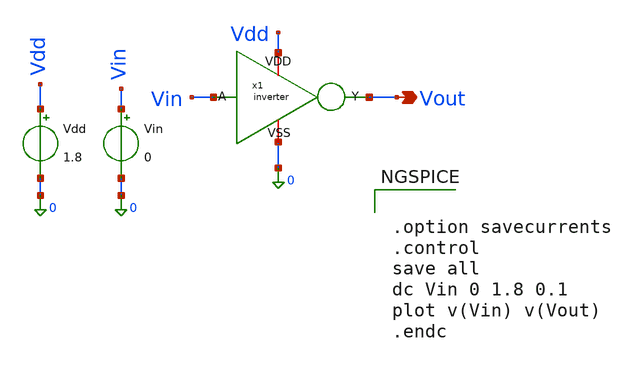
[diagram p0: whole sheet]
** sch_path: Familiarisation of IIC-OSIC-TOOLS/Test Bench/DC/inverter_tb.sch
**.subckt inverter_tb Vout
*.opin Vout
x1 Vdd Vin Vout 0 inverter
Vin Vin 0 0
Vdd Vdd 0 1.8
**** begin user architecture code

** opencircuitdesign pdks install
.lib $::SKYWATER_MODELS/sky130.lib.spice tt



.option savecurrents
.control
save all
dc Vin 0 1.8 0.1
plot v(Vin) v(Vout)
.endc


**** end user architecture code
**.ends
.end
